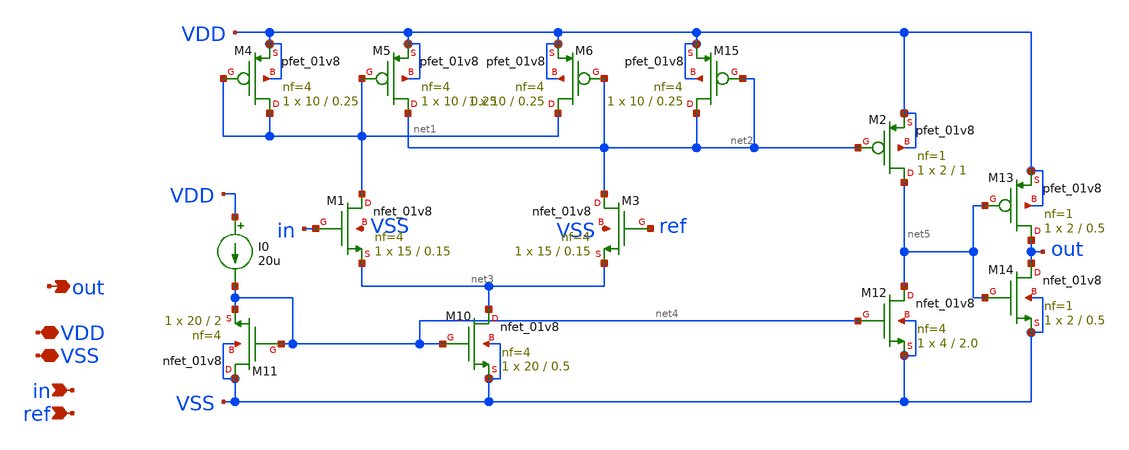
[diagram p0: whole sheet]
** sch_path: xschem/src/comparator2/comparator2_10mv_hysteresis.sch
**.subckt comparator2_10mv_hysteresis VDD in out VSS ref
*.iopin VDD
*.ipin in
*.opin out
*.iopin VSS
*.ipin ref
XM4 net1 net1 VDD VDD sky130_fd_pr__pfet_01v8 L=0.25 W=10 nf=4 ad='int((nf+1)/2) * W/nf * 0.29' as='int((nf+2)/2) * W/nf * 0.29'
+ pd='2*int((nf+1)/2) * (W/nf + 0.29)' ps='2*int((nf+2)/2) * (W/nf + 0.29)' nrd='0.29 / W' nrs='0.29 / W'
+ sa=0 sb=0 sd=0 mult=1 m=1
XM5 net2 net1 VDD VDD sky130_fd_pr__pfet_01v8 L=0.25 W=10 nf=4 ad='int((nf+1)/2) * W/nf * 0.29' as='int((nf+2)/2) * W/nf * 0.29'
+ pd='2*int((nf+1)/2) * (W/nf + 0.29)' ps='2*int((nf+2)/2) * (W/nf + 0.29)' nrd='0.29 / W' nrs='0.29 / W'
+ sa=0 sb=0 sd=0 mult=1 m=1
XM6 net1 net2 VDD VDD sky130_fd_pr__pfet_01v8 L=0.25 W=10 nf=4 ad='int((nf+1)/2) * W/nf * 0.29' as='int((nf+2)/2) * W/nf * 0.29'
+ pd='2*int((nf+1)/2) * (W/nf + 0.29)' ps='2*int((nf+2)/2) * (W/nf + 0.29)' nrd='0.29 / W' nrs='0.29 / W'
+ sa=0 sb=0 sd=0 mult=1 m=1
XM10 net3 net4 VSS VSS sky130_fd_pr__nfet_01v8 L=0.5 W=20 nf=4 ad='int((nf+1)/2) * W/nf * 0.29' as='int((nf+2)/2) * W/nf * 0.29'
+ pd='2*int((nf+1)/2) * (W/nf + 0.29)' ps='2*int((nf+2)/2) * (W/nf + 0.29)' nrd='0.29 / W' nrs='0.29 / W'
+ sa=0 sb=0 sd=0 mult=1 m=1
XM11 VSS net4 net4 VSS sky130_fd_pr__nfet_01v8 L=2 W=20 nf=4 ad='int((nf+1)/2) * W/nf * 0.29' as='int((nf+2)/2) * W/nf * 0.29'
+ pd='2*int((nf+1)/2) * (W/nf + 0.29)' ps='2*int((nf+2)/2) * (W/nf + 0.29)' nrd='0.29 / W' nrs='0.29 / W'
+ sa=0 sb=0 sd=0 mult=1 m=1
XM12 net5 net4 VSS VSS sky130_fd_pr__nfet_01v8 L=2.0 W=4 nf=4 ad='int((nf+1)/2) * W/nf * 0.29' as='int((nf+2)/2) * W/nf * 0.29'
+ pd='2*int((nf+1)/2) * (W/nf + 0.29)' ps='2*int((nf+2)/2) * (W/nf + 0.29)' nrd='0.29 / W' nrs='0.29 / W'
+ sa=0 sb=0 sd=0 mult=1 m=1
XM13 out net5 VDD VDD sky130_fd_pr__pfet_01v8 L=0.5 W=2 nf=1 ad='int((nf+1)/2) * W/nf * 0.29' as='int((nf+2)/2) * W/nf * 0.29'
+ pd='2*int((nf+1)/2) * (W/nf + 0.29)' ps='2*int((nf+2)/2) * (W/nf + 0.29)' nrd='0.29 / W' nrs='0.29 / W'
+ sa=0 sb=0 sd=0 mult=1 m=1
XM14 out net5 VSS VSS sky130_fd_pr__nfet_01v8 L=0.5 W=2 nf=1 ad='int((nf+1)/2) * W/nf * 0.29' as='int((nf+2)/2) * W/nf * 0.29'
+ pd='2*int((nf+1)/2) * (W/nf + 0.29)' ps='2*int((nf+2)/2) * (W/nf + 0.29)' nrd='0.29 / W' nrs='0.29 / W'
+ sa=0 sb=0 sd=0 mult=1 m=1
XM15 net2 net2 VDD VDD sky130_fd_pr__pfet_01v8 L=0.25 W=10 nf=4 ad='int((nf+1)/2) * W/nf * 0.29' as='int((nf+2)/2) * W/nf * 0.29'
+ pd='2*int((nf+1)/2) * (W/nf + 0.29)' ps='2*int((nf+2)/2) * (W/nf + 0.29)' nrd='0.29 / W' nrs='0.29 / W'
+ sa=0 sb=0 sd=0 mult=1 m=1
I0 VDD net4 20u
XM2 net5 net2 VDD VDD sky130_fd_pr__pfet_01v8 L=1 W=2 nf=1 ad='int((nf+1)/2) * W/nf * 0.29' as='int((nf+2)/2) * W/nf * 0.29'
+ pd='2*int((nf+1)/2) * (W/nf + 0.29)' ps='2*int((nf+2)/2) * (W/nf + 0.29)' nrd='0.29 / W' nrs='0.29 / W'
+ sa=0 sb=0 sd=0 mult=1 m=1
XM1 net1 in net3 VSS sky130_fd_pr__nfet_01v8 L=0.15 W=15 nf=4 ad='int((nf+1)/2) * W/nf * 0.29' as='int((nf+2)/2) * W/nf * 0.29'
+ pd='2*int((nf+1)/2) * (W/nf + 0.29)' ps='2*int((nf+2)/2) * (W/nf + 0.29)' nrd='0.29 / W' nrs='0.29 / W'
+ sa=0 sb=0 sd=0 mult=1 m=1
XM3 net2 ref net3 VSS sky130_fd_pr__nfet_01v8 L=0.15 W=15 nf=4 ad='int((nf+1)/2) * W/nf * 0.29' as='int((nf+2)/2) * W/nf * 0.29'
+ pd='2*int((nf+1)/2) * (W/nf + 0.29)' ps='2*int((nf+2)/2) * (W/nf + 0.29)' nrd='0.29 / W' nrs='0.29 / W'
+ sa=0 sb=0 sd=0 mult=1 m=1
**.ends
.end
